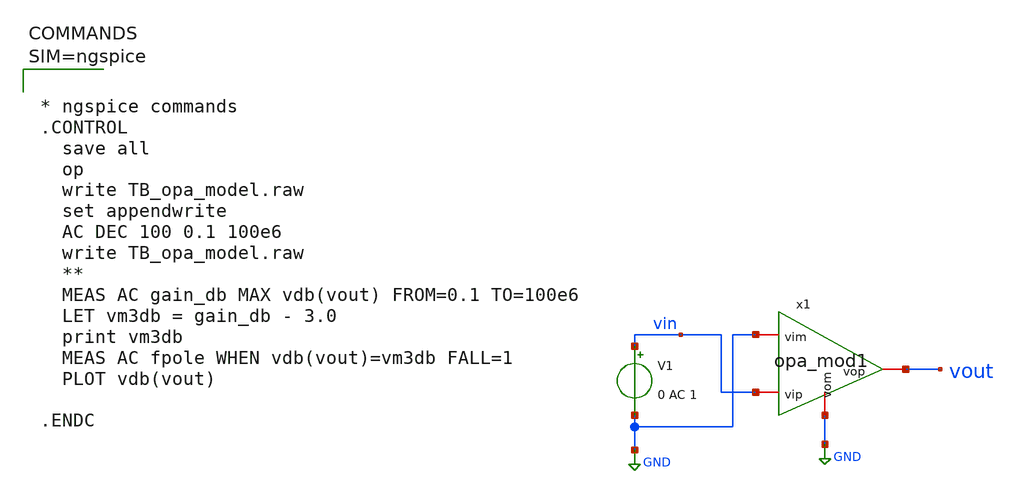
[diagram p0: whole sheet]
** sch_path: xschem/TB_opa_model.sch
**.subckt TB_opa_model
x1 vout vin GND GND opa_mod1
V1 vin GND 0 AC 1
**** begin user architecture code



* ngspice commands
.CONTROL
  save all
  op
  write TB_opa_model.raw
  set appendwrite
  AC DEC 100 0.1 100e6
  write TB_opa_model.raw
  **
  MEAS AC gain_db MAX vdb(vout) FROM=0.1 TO=100e6
  LET vm3db = gain_db - 3.0
  print vm3db
  MEAS AC fpole WHEN vdb(vout)=vm3db FALL=1
  PLOT vdb(vout)

.ENDC



**** end user architecture code
**.ends

* expanding   symbol:  opa_mod1.sym # of pins=4
** sym_path: xschem/opa_mod1.sym
** sch_path: xschem/opa_mod1.sch
.subckt opa_mod1 vop vip vim vom
*.iopin vop
*.iopin vom
*.iopin vip
*.iopin vim
E1 vilp GND vip vim 1000
R1 vilp volp 200 m=1
C1 volp GND 1u m=1
E2 vop vom volp GND 1
.ends

.GLOBAL GND
.end
